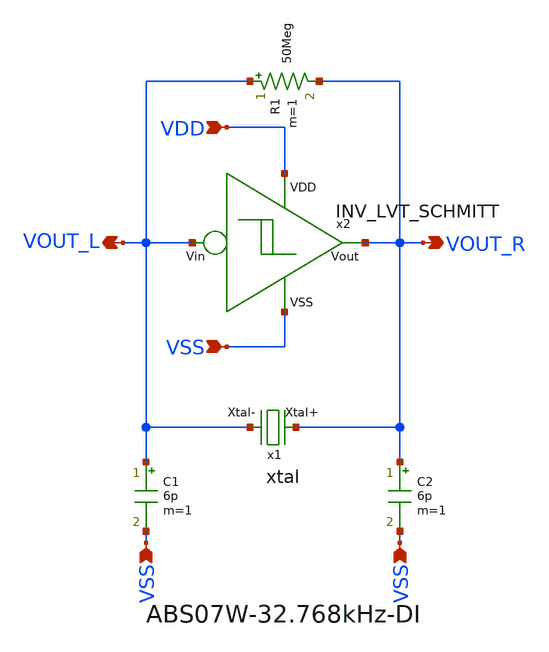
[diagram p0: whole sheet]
** sch_path: design/THESIS_EXP_RO_INVERTER_SKY130A/xtal_osc_schmitt.sch
**.subckt xtal_osc_schmitt VDD VSS VSS VSS VOUT_R VOUT_L
*.ipin VDD
*.ipin VSS
*.ipin VSS
*.ipin VSS
*.opin VOUT_R
*.opin VOUT_L
x1 VOUT_R VOUT_L xtal
C1 VOUT_L VSS 6p m=1
C2 VOUT_R VSS 6p m=1
R1 VOUT_L VOUT_R 50Meg m=1
x2 VDD VSS VOUT_R VOUT_L INV_LVT_SCHMITT
**.ends

* expanding   symbol:  THESIS_EXP_RO_INVERTER_SKY130A/xtal.sym # of pins=2
** sym_path: design/THESIS_EXP_RO_INVERTER_SKY130A/xtal.sym
** sch_path: design/THESIS_EXP_RO_INVERTER_SKY130A/xtal.sch
.subckt xtal Xtal+ Xtal-
*.iopin Xtal+
*.iopin Xtal-
R1 Xtal+ net1 38.194k m=1
C1 net1 net2 4.68f m=1
L1 net2 Xtal- 5048.571 m=1
C2 Xtal+ Xtal- 1.15p m=1
.ends


* expanding   symbol:  THESIS_EXP_RO_INVERTER_SKY130A/INV_LVT_SCHMITT.sym # of pins=4
** sym_path: design/THESIS_EXP_RO_INVERTER_SKY130A/INV_LVT_SCHMITT.sym
** sch_path: design/THESIS_EXP_RO_INVERTER_SKY130A/INV_LVT_SCHMITT.sch
.subckt INV_LVT_SCHMITT VDD VSS Vout Vin
*.ipin VSS
*.ipin Vin
*.opin Vout
*.ipin VDD
XM1[55] net1[13] Vin VDD VDD sky130_fd_pr__pfet_01v8_lvt L=1 W=7 nf=1 ad='int((nf+1)/2) * W/nf * 0.29'
+ as='int((nf+2)/2) * W/nf * 0.29' pd='2*int((nf+1)/2) * (W/nf + 0.29)' ps='2*int((nf+2)/2) * (W/nf + 0.29)'
+ nrd='0.29 / W' nrs='0.29 / W' sa=0 sb=0 sd=0 mult=1 m=1
XM1[54] net1[12] Vin VDD VDD sky130_fd_pr__pfet_01v8_lvt L=1 W=7 nf=1 ad='int((nf+1)/2) * W/nf * 0.29'
+ as='int((nf+2)/2) * W/nf * 0.29' pd='2*int((nf+1)/2) * (W/nf + 0.29)' ps='2*int((nf+2)/2) * (W/nf + 0.29)'
+ nrd='0.29 / W' nrs='0.29 / W' sa=0 sb=0 sd=0 mult=1 m=1
XM1[53] net1[11] Vin VDD VDD sky130_fd_pr__pfet_01v8_lvt L=1 W=7 nf=1 ad='int((nf+1)/2) * W/nf * 0.29'
+ as='int((nf+2)/2) * W/nf * 0.29' pd='2*int((nf+1)/2) * (W/nf + 0.29)' ps='2*int((nf+2)/2) * (W/nf + 0.29)'
+ nrd='0.29 / W' nrs='0.29 / W' sa=0 sb=0 sd=0 mult=1 m=1
XM1[52] net1[10] Vin VDD VDD sky130_fd_pr__pfet_01v8_lvt L=1 W=7 nf=1 ad='int((nf+1)/2) * W/nf * 0.29'
+ as='int((nf+2)/2) * W/nf * 0.29' pd='2*int((nf+1)/2) * (W/nf + 0.29)' ps='2*int((nf+2)/2) * (W/nf + 0.29)'
+ nrd='0.29 / W' nrs='0.29 / W' sa=0 sb=0 sd=0 mult=1 m=1
XM1[51] net1[9] Vin VDD VDD sky130_fd_pr__pfet_01v8_lvt L=1 W=7 nf=1 ad='int((nf+1)/2) * W/nf * 0.29'
+ as='int((nf+2)/2) * W/nf * 0.29' pd='2*int((nf+1)/2) * (W/nf + 0.29)' ps='2*int((nf+2)/2) * (W/nf + 0.29)'
+ nrd='0.29 / W' nrs='0.29 / W' sa=0 sb=0 sd=0 mult=1 m=1
XM1[50] net1[8] Vin VDD VDD sky130_fd_pr__pfet_01v8_lvt L=1 W=7 nf=1 ad='int((nf+1)/2) * W/nf * 0.29'
+ as='int((nf+2)/2) * W/nf * 0.29' pd='2*int((nf+1)/2) * (W/nf + 0.29)' ps='2*int((nf+2)/2) * (W/nf + 0.29)'
+ nrd='0.29 / W' nrs='0.29 / W' sa=0 sb=0 sd=0 mult=1 m=1
XM1[49] net1[7] Vin VDD VDD sky130_fd_pr__pfet_01v8_lvt L=1 W=7 nf=1 ad='int((nf+1)/2) * W/nf * 0.29'
+ as='int((nf+2)/2) * W/nf * 0.29' pd='2*int((nf+1)/2) * (W/nf + 0.29)' ps='2*int((nf+2)/2) * (W/nf + 0.29)'
+ nrd='0.29 / W' nrs='0.29 / W' sa=0 sb=0 sd=0 mult=1 m=1
XM1[48] net1[6] Vin VDD VDD sky130_fd_pr__pfet_01v8_lvt L=1 W=7 nf=1 ad='int((nf+1)/2) * W/nf * 0.29'
+ as='int((nf+2)/2) * W/nf * 0.29' pd='2*int((nf+1)/2) * (W/nf + 0.29)' ps='2*int((nf+2)/2) * (W/nf + 0.29)'
+ nrd='0.29 / W' nrs='0.29 / W' sa=0 sb=0 sd=0 mult=1 m=1
XM1[47] net1[5] Vin VDD VDD sky130_fd_pr__pfet_01v8_lvt L=1 W=7 nf=1 ad='int((nf+1)/2) * W/nf * 0.29'
+ as='int((nf+2)/2) * W/nf * 0.29' pd='2*int((nf+1)/2) * (W/nf + 0.29)' ps='2*int((nf+2)/2) * (W/nf + 0.29)'
+ nrd='0.29 / W' nrs='0.29 / W' sa=0 sb=0 sd=0 mult=1 m=1
XM1[46] net1[4] Vin VDD VDD sky130_fd_pr__pfet_01v8_lvt L=1 W=7 nf=1 ad='int((nf+1)/2) * W/nf * 0.29'
+ as='int((nf+2)/2) * W/nf * 0.29' pd='2*int((nf+1)/2) * (W/nf + 0.29)' ps='2*int((nf+2)/2) * (W/nf + 0.29)'
+ nrd='0.29 / W' nrs='0.29 / W' sa=0 sb=0 sd=0 mult=1 m=1
XM1[45] net1[3] Vin VDD VDD sky130_fd_pr__pfet_01v8_lvt L=1 W=7 nf=1 ad='int((nf+1)/2) * W/nf * 0.29'
+ as='int((nf+2)/2) * W/nf * 0.29' pd='2*int((nf+1)/2) * (W/nf + 0.29)' ps='2*int((nf+2)/2) * (W/nf + 0.29)'
+ nrd='0.29 / W' nrs='0.29 / W' sa=0 sb=0 sd=0 mult=1 m=1
XM1[44] net1[2] Vin VDD VDD sky130_fd_pr__pfet_01v8_lvt L=1 W=7 nf=1 ad='int((nf+1)/2) * W/nf * 0.29'
+ as='int((nf+2)/2) * W/nf * 0.29' pd='2*int((nf+1)/2) * (W/nf + 0.29)' ps='2*int((nf+2)/2) * (W/nf + 0.29)'
+ nrd='0.29 / W' nrs='0.29 / W' sa=0 sb=0 sd=0 mult=1 m=1
XM1[43] net1[1] Vin VDD VDD sky130_fd_pr__pfet_01v8_lvt L=1 W=7 nf=1 ad='int((nf+1)/2) * W/nf * 0.29'
+ as='int((nf+2)/2) * W/nf * 0.29' pd='2*int((nf+1)/2) * (W/nf + 0.29)' ps='2*int((nf+2)/2) * (W/nf + 0.29)'
+ nrd='0.29 / W' nrs='0.29 / W' sa=0 sb=0 sd=0 mult=1 m=1
XM1[42] net1[0] Vin VDD VDD sky130_fd_pr__pfet_01v8_lvt L=1 W=7 nf=1 ad='int((nf+1)/2) * W/nf * 0.29'
+ as='int((nf+2)/2) * W/nf * 0.29' pd='2*int((nf+1)/2) * (W/nf + 0.29)' ps='2*int((nf+2)/2) * (W/nf + 0.29)'
+ nrd='0.29 / W' nrs='0.29 / W' sa=0 sb=0 sd=0 mult=1 m=1
XM1[41] net1[13] Vin VDD VDD sky130_fd_pr__pfet_01v8_lvt L=1 W=7 nf=1 ad='int((nf+1)/2) * W/nf * 0.29'
+ as='int((nf+2)/2) * W/nf * 0.29' pd='2*int((nf+1)/2) * (W/nf + 0.29)' ps='2*int((nf+2)/2) * (W/nf + 0.29)'
+ nrd='0.29 / W' nrs='0.29 / W' sa=0 sb=0 sd=0 mult=1 m=1
XM1[40] net1[12] Vin VDD VDD sky130_fd_pr__pfet_01v8_lvt L=1 W=7 nf=1 ad='int((nf+1)/2) * W/nf * 0.29'
+ as='int((nf+2)/2) * W/nf * 0.29' pd='2*int((nf+1)/2) * (W/nf + 0.29)' ps='2*int((nf+2)/2) * (W/nf + 0.29)'
+ nrd='0.29 / W' nrs='0.29 / W' sa=0 sb=0 sd=0 mult=1 m=1
XM1[39] net1[11] Vin VDD VDD sky130_fd_pr__pfet_01v8_lvt L=1 W=7 nf=1 ad='int((nf+1)/2) * W/nf * 0.29'
+ as='int((nf+2)/2) * W/nf * 0.29' pd='2*int((nf+1)/2) * (W/nf + 0.29)' ps='2*int((nf+2)/2) * (W/nf + 0.29)'
+ nrd='0.29 / W' nrs='0.29 / W' sa=0 sb=0 sd=0 mult=1 m=1
XM1[38] net1[10] Vin VDD VDD sky130_fd_pr__pfet_01v8_lvt L=1 W=7 nf=1 ad='int((nf+1)/2) * W/nf * 0.29'
+ as='int((nf+2)/2) * W/nf * 0.29' pd='2*int((nf+1)/2) * (W/nf + 0.29)' ps='2*int((nf+2)/2) * (W/nf + 0.29)'
+ nrd='0.29 / W' nrs='0.29 / W' sa=0 sb=0 sd=0 mult=1 m=1
XM1[37] net1[9] Vin VDD VDD sky130_fd_pr__pfet_01v8_lvt L=1 W=7 nf=1 ad='int((nf+1)/2) * W/nf * 0.29'
+ as='int((nf+2)/2) * W/nf * 0.29' pd='2*int((nf+1)/2) * (W/nf + 0.29)' ps='2*int((nf+2)/2) * (W/nf + 0.29)'
+ nrd='0.29 / W' nrs='0.29 / W' sa=0 sb=0 sd=0 mult=1 m=1
XM1[36] net1[8] Vin VDD VDD sky130_fd_pr__pfet_01v8_lvt L=1 W=7 nf=1 ad='int((nf+1)/2) * W/nf * 0.29'
+ as='int((nf+2)/2) * W/nf * 0.29' pd='2*int((nf+1)/2) * (W/nf + 0.29)' ps='2*int((nf+2)/2) * (W/nf + 0.29)'
+ nrd='0.29 / W' nrs='0.29 / W' sa=0 sb=0 sd=0 mult=1 m=1
XM1[35] net1[7] Vin VDD VDD sky130_fd_pr__pfet_01v8_lvt L=1 W=7 nf=1 ad='int((nf+1)/2) * W/nf * 0.29'
+ as='int((nf+2)/2) * W/nf * 0.29' pd='2*int((nf+1)/2) * (W/nf + 0.29)' ps='2*int((nf+2)/2) * (W/nf + 0.29)'
+ nrd='0.29 / W' nrs='0.29 / W' sa=0 sb=0 sd=0 mult=1 m=1
XM1[34] net1[6] Vin VDD VDD sky130_fd_pr__pfet_01v8_lvt L=1 W=7 nf=1 ad='int((nf+1)/2) * W/nf * 0.29'
+ as='int((nf+2)/2) * W/nf * 0.29' pd='2*int((nf+1)/2) * (W/nf + 0.29)' ps='2*int((nf+2)/2) * (W/nf + 0.29)'
+ nrd='0.29 / W' nrs='0.29 / W' sa=0 sb=0 sd=0 mult=1 m=1
XM1[33] net1[5] Vin VDD VDD sky130_fd_pr__pfet_01v8_lvt L=1 W=7 nf=1 ad='int((nf+1)/2) * W/nf * 0.29'
+ as='int((nf+2)/2) * W/nf * 0.29' pd='2*int((nf+1)/2) * (W/nf + 0.29)' ps='2*int((nf+2)/2) * (W/nf + 0.29)'
+ nrd='0.29 / W' nrs='0.29 / W' sa=0 sb=0 sd=0 mult=1 m=1
XM1[32] net1[4] Vin VDD VDD sky130_fd_pr__pfet_01v8_lvt L=1 W=7 nf=1 ad='int((nf+1)/2) * W/nf * 0.29'
+ as='int((nf+2)/2) * W/nf * 0.29' pd='2*int((nf+1)/2) * (W/nf + 0.29)' ps='2*int((nf+2)/2) * (W/nf + 0.29)'
+ nrd='0.29 / W' nrs='0.29 / W' sa=0 sb=0 sd=0 mult=1 m=1
XM1[31] net1[3] Vin VDD VDD sky130_fd_pr__pfet_01v8_lvt L=1 W=7 nf=1 ad='int((nf+1)/2) * W/nf * 0.29'
+ as='int((nf+2)/2) * W/nf * 0.29' pd='2*int((nf+1)/2) * (W/nf + 0.29)' ps='2*int((nf+2)/2) * (W/nf + 0.29)'
+ nrd='0.29 / W' nrs='0.29 / W' sa=0 sb=0 sd=0 mult=1 m=1
XM1[30] net1[2] Vin VDD VDD sky130_fd_pr__pfet_01v8_lvt L=1 W=7 nf=1 ad='int((nf+1)/2) * W/nf * 0.29'
+ as='int((nf+2)/2) * W/nf * 0.29' pd='2*int((nf+1)/2) * (W/nf + 0.29)' ps='2*int((nf+2)/2) * (W/nf + 0.29)'
+ nrd='0.29 / W' nrs='0.29 / W' sa=0 sb=0 sd=0 mult=1 m=1
XM1[29] net1[1] Vin VDD VDD sky130_fd_pr__pfet_01v8_lvt L=1 W=7 nf=1 ad='int((nf+1)/2) * W/nf * 0.29'
+ as='int((nf+2)/2) * W/nf * 0.29' pd='2*int((nf+1)/2) * (W/nf + 0.29)' ps='2*int((nf+2)/2) * (W/nf + 0.29)'
+ nrd='0.29 / W' nrs='0.29 / W' sa=0 sb=0 sd=0 mult=1 m=1
XM1[28] net1[0] Vin VDD VDD sky130_fd_pr__pfet_01v8_lvt L=1 W=7 nf=1 ad='int((nf+1)/2) * W/nf * 0.29'
+ as='int((nf+2)/2) * W/nf * 0.29' pd='2*int((nf+1)/2) * (W/nf + 0.29)' ps='2*int((nf+2)/2) * (W/nf + 0.29)'
+ nrd='0.29 / W' nrs='0.29 / W' sa=0 sb=0 sd=0 mult=1 m=1
XM1[27] net1[13] Vin VDD VDD sky130_fd_pr__pfet_01v8_lvt L=1 W=7 nf=1 ad='int((nf+1)/2) * W/nf * 0.29'
+ as='int((nf+2)/2) * W/nf * 0.29' pd='2*int((nf+1)/2) * (W/nf + 0.29)' ps='2*int((nf+2)/2) * (W/nf + 0.29)'
+ nrd='0.29 / W' nrs='0.29 / W' sa=0 sb=0 sd=0 mult=1 m=1
XM1[26] net1[12] Vin VDD VDD sky130_fd_pr__pfet_01v8_lvt L=1 W=7 nf=1 ad='int((nf+1)/2) * W/nf * 0.29'
+ as='int((nf+2)/2) * W/nf * 0.29' pd='2*int((nf+1)/2) * (W/nf + 0.29)' ps='2*int((nf+2)/2) * (W/nf + 0.29)'
+ nrd='0.29 / W' nrs='0.29 / W' sa=0 sb=0 sd=0 mult=1 m=1
XM1[25] net1[11] Vin VDD VDD sky130_fd_pr__pfet_01v8_lvt L=1 W=7 nf=1 ad='int((nf+1)/2) * W/nf * 0.29'
+ as='int((nf+2)/2) * W/nf * 0.29' pd='2*int((nf+1)/2) * (W/nf + 0.29)' ps='2*int((nf+2)/2) * (W/nf + 0.29)'
+ nrd='0.29 / W' nrs='0.29 / W' sa=0 sb=0 sd=0 mult=1 m=1
XM1[24] net1[10] Vin VDD VDD sky130_fd_pr__pfet_01v8_lvt L=1 W=7 nf=1 ad='int((nf+1)/2) * W/nf * 0.29'
+ as='int((nf+2)/2) * W/nf * 0.29' pd='2*int((nf+1)/2) * (W/nf + 0.29)' ps='2*int((nf+2)/2) * (W/nf + 0.29)'
+ nrd='0.29 / W' nrs='0.29 / W' sa=0 sb=0 sd=0 mult=1 m=1
XM1[23] net1[9] Vin VDD VDD sky130_fd_pr__pfet_01v8_lvt L=1 W=7 nf=1 ad='int((nf+1)/2) * W/nf * 0.29'
+ as='int((nf+2)/2) * W/nf * 0.29' pd='2*int((nf+1)/2) * (W/nf + 0.29)' ps='2*int((nf+2)/2) * (W/nf + 0.29)'
+ nrd='0.29 / W' nrs='0.29 / W' sa=0 sb=0 sd=0 mult=1 m=1
XM1[22] net1[8] Vin VDD VDD sky130_fd_pr__pfet_01v8_lvt L=1 W=7 nf=1 ad='int((nf+1)/2) * W/nf * 0.29'
+ as='int((nf+2)/2) * W/nf * 0.29' pd='2*int((nf+1)/2) * (W/nf + 0.29)' ps='2*int((nf+2)/2) * (W/nf + 0.29)'
+ nrd='0.29 / W' nrs='0.29 / W' sa=0 sb=0 sd=0 mult=1 m=1
XM1[21] net1[7] Vin VDD VDD sky130_fd_pr__pfet_01v8_lvt L=1 W=7 nf=1 ad='int((nf+1)/2) * W/nf * 0.29'
+ as='int((nf+2)/2) * W/nf * 0.29' pd='2*int((nf+1)/2) * (W/nf + 0.29)' ps='2*int((nf+2)/2) * (W/nf + 0.29)'
+ nrd='0.29 / W' nrs='0.29 / W' sa=0 sb=0 sd=0 mult=1 m=1
XM1[20] net1[6] Vin VDD VDD sky130_fd_pr__pfet_01v8_lvt L=1 W=7 nf=1 ad='int((nf+1)/2) * W/nf * 0.29'
+ as='int((nf+2)/2) * W/nf * 0.29' pd='2*int((nf+1)/2) * (W/nf + 0.29)' ps='2*int((nf+2)/2) * (W/nf + 0.29)'
+ nrd='0.29 / W' nrs='0.29 / W' sa=0 sb=0 sd=0 mult=1 m=1
XM1[19] net1[5] Vin VDD VDD sky130_fd_pr__pfet_01v8_lvt L=1 W=7 nf=1 ad='int((nf+1)/2) * W/nf * 0.29'
+ as='int((nf+2)/2) * W/nf * 0.29' pd='2*int((nf+1)/2) * (W/nf + 0.29)' ps='2*int((nf+2)/2) * (W/nf + 0.29)'
+ nrd='0.29 / W' nrs='0.29 / W' sa=0 sb=0 sd=0 mult=1 m=1
XM1[18] net1[4] Vin VDD VDD sky130_fd_pr__pfet_01v8_lvt L=1 W=7 nf=1 ad='int((nf+1)/2) * W/nf * 0.29'
+ as='int((nf+2)/2) * W/nf * 0.29' pd='2*int((nf+1)/2) * (W/nf + 0.29)' ps='2*int((nf+2)/2) * (W/nf + 0.29)'
+ nrd='0.29 / W' nrs='0.29 / W' sa=0 sb=0 sd=0 mult=1 m=1
XM1[17] net1[3] Vin VDD VDD sky130_fd_pr__pfet_01v8_lvt L=1 W=7 nf=1 ad='int((nf+1)/2) * W/nf * 0.29'
+ as='int((nf+2)/2) * W/nf * 0.29' pd='2*int((nf+1)/2) * (W/nf + 0.29)' ps='2*int((nf+2)/2) * (W/nf + 0.29)'
+ nrd='0.29 / W' nrs='0.29 / W' sa=0 sb=0 sd=0 mult=1 m=1
XM1[16] net1[2] Vin VDD VDD sky130_fd_pr__pfet_01v8_lvt L=1 W=7 nf=1 ad='int((nf+1)/2) * W/nf * 0.29'
+ as='int((nf+2)/2) * W/nf * 0.29' pd='2*int((nf+1)/2) * (W/nf + 0.29)' ps='2*int((nf+2)/2) * (W/nf + 0.29)'
+ nrd='0.29 / W' nrs='0.29 / W' sa=0 sb=0 sd=0 mult=1 m=1
XM1[15] net1[1] Vin VDD VDD sky130_fd_pr__pfet_01v8_lvt L=1 W=7 nf=1 ad='int((nf+1)/2) * W/nf * 0.29'
+ as='int((nf+2)/2) * W/nf * 0.29' pd='2*int((nf+1)/2) * (W/nf + 0.29)' ps='2*int((nf+2)/2) * (W/nf + 0.29)'
+ nrd='0.29 / W' nrs='0.29 / W' sa=0 sb=0 sd=0 mult=1 m=1
XM1[14] net1[0] Vin VDD VDD sky130_fd_pr__pfet_01v8_lvt L=1 W=7 nf=1 ad='int((nf+1)/2) * W/nf * 0.29'
+ as='int((nf+2)/2) * W/nf * 0.29' pd='2*int((nf+1)/2) * (W/nf + 0.29)' ps='2*int((nf+2)/2) * (W/nf + 0.29)'
+ nrd='0.29 / W' nrs='0.29 / W' sa=0 sb=0 sd=0 mult=1 m=1
XM1[13] net1[13] Vin VDD VDD sky130_fd_pr__pfet_01v8_lvt L=1 W=7 nf=1 ad='int((nf+1)/2) * W/nf * 0.29'
+ as='int((nf+2)/2) * W/nf * 0.29' pd='2*int((nf+1)/2) * (W/nf + 0.29)' ps='2*int((nf+2)/2) * (W/nf + 0.29)'
+ nrd='0.29 / W' nrs='0.29 / W' sa=0 sb=0 sd=0 mult=1 m=1
XM1[12] net1[12] Vin VDD VDD sky130_fd_pr__pfet_01v8_lvt L=1 W=7 nf=1 ad='int((nf+1)/2) * W/nf * 0.29'
+ as='int((nf+2)/2) * W/nf * 0.29' pd='2*int((nf+1)/2) * (W/nf + 0.29)' ps='2*int((nf+2)/2) * (W/nf + 0.29)'
+ nrd='0.29 / W' nrs='0.29 / W' sa=0 sb=0 sd=0 mult=1 m=1
XM1[11] net1[11] Vin VDD VDD sky130_fd_pr__pfet_01v8_lvt L=1 W=7 nf=1 ad='int((nf+1)/2) * W/nf * 0.29'
+ as='int((nf+2)/2) * W/nf * 0.29' pd='2*int((nf+1)/2) * (W/nf + 0.29)' ps='2*int((nf+2)/2) * (W/nf + 0.29)'
+ nrd='0.29 / W' nrs='0.29 / W' sa=0 sb=0 sd=0 mult=1 m=1
XM1[10] net1[10] Vin VDD VDD sky130_fd_pr__pfet_01v8_lvt L=1 W=7 nf=1 ad='int((nf+1)/2) * W/nf * 0.29'
+ as='int((nf+2)/2) * W/nf * 0.29' pd='2*int((nf+1)/2) * (W/nf + 0.29)' ps='2*int((nf+2)/2) * (W/nf + 0.29)'
+ nrd='0.29 / W' nrs='0.29 / W' sa=0 sb=0 sd=0 mult=1 m=1
XM1[9] net1[9] Vin VDD VDD sky130_fd_pr__pfet_01v8_lvt L=1 W=7 nf=1 ad='int((nf+1)/2) * W/nf * 0.29'
+ as='int((nf+2)/2) * W/nf * 0.29' pd='2*int((nf+1)/2) * (W/nf + 0.29)' ps='2*int((nf+2)/2) * (W/nf + 0.29)'
+ nrd='0.29 / W' nrs='0.29 / W' sa=0 sb=0 sd=0 mult=1 m=1
XM1[8] net1[8] Vin VDD VDD sky130_fd_pr__pfet_01v8_lvt L=1 W=7 nf=1 ad='int((nf+1)/2) * W/nf * 0.29'
+ as='int((nf+2)/2) * W/nf * 0.29' pd='2*int((nf+1)/2) * (W/nf + 0.29)' ps='2*int((nf+2)/2) * (W/nf + 0.29)'
+ nrd='0.29 / W' nrs='0.29 / W' sa=0 sb=0 sd=0 mult=1 m=1
XM1[7] net1[7] Vin VDD VDD sky130_fd_pr__pfet_01v8_lvt L=1 W=7 nf=1 ad='int((nf+1)/2) * W/nf * 0.29'
+ as='int((nf+2)/2) * W/nf * 0.29' pd='2*int((nf+1)/2) * (W/nf + 0.29)' ps='2*int((nf+2)/2) * (W/nf + 0.29)'
+ nrd='0.29 / W' nrs='0.29 / W' sa=0 sb=0 sd=0 mult=1 m=1
XM1[6] net1[6] Vin VDD VDD sky130_fd_pr__pfet_01v8_lvt L=1 W=7 nf=1 ad='int((nf+1)/2) * W/nf * 0.29'
+ as='int((nf+2)/2) * W/nf * 0.29' pd='2*int((nf+1)/2) * (W/nf + 0.29)' ps='2*int((nf+2)/2) * (W/nf + 0.29)'
+ nrd='0.29 / W' nrs='0.29 / W' sa=0 sb=0 sd=0 mult=1 m=1
XM1[5] net1[5] Vin VDD VDD sky130_fd_pr__pfet_01v8_lvt L=1 W=7 nf=1 ad='int((nf+1)/2) * W/nf * 0.29'
+ as='int((nf+2)/2) * W/nf * 0.29' pd='2*int((nf+1)/2) * (W/nf + 0.29)' ps='2*int((nf+2)/2) * (W/nf + 0.29)'
+ nrd='0.29 / W' nrs='0.29 / W' sa=0 sb=0 sd=0 mult=1 m=1
XM1[4] net1[4] Vin VDD VDD sky130_fd_pr__pfet_01v8_lvt L=1 W=7 nf=1 ad='int((nf+1)/2) * W/nf * 0.29'
+ as='int((nf+2)/2) * W/nf * 0.29' pd='2*int((nf+1)/2) * (W/nf + 0.29)' ps='2*int((nf+2)/2) * (W/nf + 0.29)'
+ nrd='0.29 / W' nrs='0.29 / W' sa=0 sb=0 sd=0 mult=1 m=1
XM1[3] net1[3] Vin VDD VDD sky130_fd_pr__pfet_01v8_lvt L=1 W=7 nf=1 ad='int((nf+1)/2) * W/nf * 0.29'
+ as='int((nf+2)/2) * W/nf * 0.29' pd='2*int((nf+1)/2) * (W/nf + 0.29)' ps='2*int((nf+2)/2) * (W/nf + 0.29)'
+ nrd='0.29 / W' nrs='0.29 / W' sa=0 sb=0 sd=0 mult=1 m=1
XM1[2] net1[2] Vin VDD VDD sky130_fd_pr__pfet_01v8_lvt L=1 W=7 nf=1 ad='int((nf+1)/2) * W/nf * 0.29'
+ as='int((nf+2)/2) * W/nf * 0.29' pd='2*int((nf+1)/2) * (W/nf + 0.29)' ps='2*int((nf+2)/2) * (W/nf + 0.29)'
+ nrd='0.29 / W' nrs='0.29 / W' sa=0 sb=0 sd=0 mult=1 m=1
XM1[1] net1[1] Vin VDD VDD sky130_fd_pr__pfet_01v8_lvt L=1 W=7 nf=1 ad='int((nf+1)/2) * W/nf * 0.29'
+ as='int((nf+2)/2) * W/nf * 0.29' pd='2*int((nf+1)/2) * (W/nf + 0.29)' ps='2*int((nf+2)/2) * (W/nf + 0.29)'
+ nrd='0.29 / W' nrs='0.29 / W' sa=0 sb=0 sd=0 mult=1 m=1
XM1[0] net1[0] Vin VDD VDD sky130_fd_pr__pfet_01v8_lvt L=1 W=7 nf=1 ad='int((nf+1)/2) * W/nf * 0.29'
+ as='int((nf+2)/2) * W/nf * 0.29' pd='2*int((nf+1)/2) * (W/nf + 0.29)' ps='2*int((nf+2)/2) * (W/nf + 0.29)'
+ nrd='0.29 / W' nrs='0.29 / W' sa=0 sb=0 sd=0 mult=1 m=1
XM2[13] Vout Vin net1[13] VDD sky130_fd_pr__pfet_01v8_lvt L=1 W=7 nf=1 ad='int((nf+1)/2) * W/nf * 0.29'
+ as='int((nf+2)/2) * W/nf * 0.29' pd='2*int((nf+1)/2) * (W/nf + 0.29)' ps='2*int((nf+2)/2) * (W/nf + 0.29)'
+ nrd='0.29 / W' nrs='0.29 / W' sa=0 sb=0 sd=0 mult=1 m=1
XM2[12] Vout Vin net1[12] VDD sky130_fd_pr__pfet_01v8_lvt L=1 W=7 nf=1 ad='int((nf+1)/2) * W/nf * 0.29'
+ as='int((nf+2)/2) * W/nf * 0.29' pd='2*int((nf+1)/2) * (W/nf + 0.29)' ps='2*int((nf+2)/2) * (W/nf + 0.29)'
+ nrd='0.29 / W' nrs='0.29 / W' sa=0 sb=0 sd=0 mult=1 m=1
XM2[11] Vout Vin net1[11] VDD sky130_fd_pr__pfet_01v8_lvt L=1 W=7 nf=1 ad='int((nf+1)/2) * W/nf * 0.29'
+ as='int((nf+2)/2) * W/nf * 0.29' pd='2*int((nf+1)/2) * (W/nf + 0.29)' ps='2*int((nf+2)/2) * (W/nf + 0.29)'
+ nrd='0.29 / W' nrs='0.29 / W' sa=0 sb=0 sd=0 mult=1 m=1
XM2[10] Vout Vin net1[10] VDD sky130_fd_pr__pfet_01v8_lvt L=1 W=7 nf=1 ad='int((nf+1)/2) * W/nf * 0.29'
+ as='int((nf+2)/2) * W/nf * 0.29' pd='2*int((nf+1)/2) * (W/nf + 0.29)' ps='2*int((nf+2)/2) * (W/nf + 0.29)'
+ nrd='0.29 / W' nrs='0.29 / W' sa=0 sb=0 sd=0 mult=1 m=1
XM2[9] Vout Vin net1[9] VDD sky130_fd_pr__pfet_01v8_lvt L=1 W=7 nf=1 ad='int((nf+1)/2) * W/nf * 0.29'
+ as='int((nf+2)/2) * W/nf * 0.29' pd='2*int((nf+1)/2) * (W/nf + 0.29)' ps='2*int((nf+2)/2) * (W/nf + 0.29)'
+ nrd='0.29 / W' nrs='0.29 / W' sa=0 sb=0 sd=0 mult=1 m=1
XM2[8] Vout Vin net1[8] VDD sky130_fd_pr__pfet_01v8_lvt L=1 W=7 nf=1 ad='int((nf+1)/2) * W/nf * 0.29'
+ as='int((nf+2)/2) * W/nf * 0.29' pd='2*int((nf+1)/2) * (W/nf + 0.29)' ps='2*int((nf+2)/2) * (W/nf + 0.29)'
+ nrd='0.29 / W' nrs='0.29 / W' sa=0 sb=0 sd=0 mult=1 m=1
XM2[7] Vout Vin net1[7] VDD sky130_fd_pr__pfet_01v8_lvt L=1 W=7 nf=1 ad='int((nf+1)/2) * W/nf * 0.29'
+ as='int((nf+2)/2) * W/nf * 0.29' pd='2*int((nf+1)/2) * (W/nf + 0.29)' ps='2*int((nf+2)/2) * (W/nf + 0.29)'
+ nrd='0.29 / W' nrs='0.29 / W' sa=0 sb=0 sd=0 mult=1 m=1
XM2[6] Vout Vin net1[6] VDD sky130_fd_pr__pfet_01v8_lvt L=1 W=7 nf=1 ad='int((nf+1)/2) * W/nf * 0.29'
+ as='int((nf+2)/2) * W/nf * 0.29' pd='2*int((nf+1)/2) * (W/nf + 0.29)' ps='2*int((nf+2)/2) * (W/nf + 0.29)'
+ nrd='0.29 / W' nrs='0.29 / W' sa=0 sb=0 sd=0 mult=1 m=1
XM2[5] Vout Vin net1[5] VDD sky130_fd_pr__pfet_01v8_lvt L=1 W=7 nf=1 ad='int((nf+1)/2) * W/nf * 0.29'
+ as='int((nf+2)/2) * W/nf * 0.29' pd='2*int((nf+1)/2) * (W/nf + 0.29)' ps='2*int((nf+2)/2) * (W/nf + 0.29)'
+ nrd='0.29 / W' nrs='0.29 / W' sa=0 sb=0 sd=0 mult=1 m=1
XM2[4] Vout Vin net1[4] VDD sky130_fd_pr__pfet_01v8_lvt L=1 W=7 nf=1 ad='int((nf+1)/2) * W/nf * 0.29'
+ as='int((nf+2)/2) * W/nf * 0.29' pd='2*int((nf+1)/2) * (W/nf + 0.29)' ps='2*int((nf+2)/2) * (W/nf + 0.29)'
+ nrd='0.29 / W' nrs='0.29 / W' sa=0 sb=0 sd=0 mult=1 m=1
XM2[3] Vout Vin net1[3] VDD sky130_fd_pr__pfet_01v8_lvt L=1 W=7 nf=1 ad='int((nf+1)/2) * W/nf * 0.29'
+ as='int((nf+2)/2) * W/nf * 0.29' pd='2*int((nf+1)/2) * (W/nf + 0.29)' ps='2*int((nf+2)/2) * (W/nf + 0.29)'
+ nrd='0.29 / W' nrs='0.29 / W' sa=0 sb=0 sd=0 mult=1 m=1
XM2[2] Vout Vin net1[2] VDD sky130_fd_pr__pfet_01v8_lvt L=1 W=7 nf=1 ad='int((nf+1)/2) * W/nf * 0.29'
+ as='int((nf+2)/2) * W/nf * 0.29' pd='2*int((nf+1)/2) * (W/nf + 0.29)' ps='2*int((nf+2)/2) * (W/nf + 0.29)'
+ nrd='0.29 / W' nrs='0.29 / W' sa=0 sb=0 sd=0 mult=1 m=1
XM2[1] Vout Vin net1[1] VDD sky130_fd_pr__pfet_01v8_lvt L=1 W=7 nf=1 ad='int((nf+1)/2) * W/nf * 0.29'
+ as='int((nf+2)/2) * W/nf * 0.29' pd='2*int((nf+1)/2) * (W/nf + 0.29)' ps='2*int((nf+2)/2) * (W/nf + 0.29)'
+ nrd='0.29 / W' nrs='0.29 / W' sa=0 sb=0 sd=0 mult=1 m=1
XM2[0] Vout Vin net1[0] VDD sky130_fd_pr__pfet_01v8_lvt L=1 W=7 nf=1 ad='int((nf+1)/2) * W/nf * 0.29'
+ as='int((nf+2)/2) * W/nf * 0.29' pd='2*int((nf+1)/2) * (W/nf + 0.29)' ps='2*int((nf+2)/2) * (W/nf + 0.29)'
+ nrd='0.29 / W' nrs='0.29 / W' sa=0 sb=0 sd=0 mult=1 m=1
XM3[27] net1[13] Vout VSS VDD sky130_fd_pr__pfet_01v8_lvt L=1 W=7 nf=1 ad='int((nf+1)/2) * W/nf * 0.29'
+ as='int((nf+2)/2) * W/nf * 0.29' pd='2*int((nf+1)/2) * (W/nf + 0.29)' ps='2*int((nf+2)/2) * (W/nf + 0.29)'
+ nrd='0.29 / W' nrs='0.29 / W' sa=0 sb=0 sd=0 mult=1 m=1
XM3[26] net1[12] Vout VSS VDD sky130_fd_pr__pfet_01v8_lvt L=1 W=7 nf=1 ad='int((nf+1)/2) * W/nf * 0.29'
+ as='int((nf+2)/2) * W/nf * 0.29' pd='2*int((nf+1)/2) * (W/nf + 0.29)' ps='2*int((nf+2)/2) * (W/nf + 0.29)'
+ nrd='0.29 / W' nrs='0.29 / W' sa=0 sb=0 sd=0 mult=1 m=1
XM3[25] net1[11] Vout VSS VDD sky130_fd_pr__pfet_01v8_lvt L=1 W=7 nf=1 ad='int((nf+1)/2) * W/nf * 0.29'
+ as='int((nf+2)/2) * W/nf * 0.29' pd='2*int((nf+1)/2) * (W/nf + 0.29)' ps='2*int((nf+2)/2) * (W/nf + 0.29)'
+ nrd='0.29 / W' nrs='0.29 / W' sa=0 sb=0 sd=0 mult=1 m=1
XM3[24] net1[10] Vout VSS VDD sky130_fd_pr__pfet_01v8_lvt L=1 W=7 nf=1 ad='int((nf+1)/2) * W/nf * 0.29'
+ as='int((nf+2)/2) * W/nf * 0.29' pd='2*int((nf+1)/2) * (W/nf + 0.29)' ps='2*int((nf+2)/2) * (W/nf + 0.29)'
+ nrd='0.29 / W' nrs='0.29 / W' sa=0 sb=0 sd=0 mult=1 m=1
XM3[23] net1[9] Vout VSS VDD sky130_fd_pr__pfet_01v8_lvt L=1 W=7 nf=1 ad='int((nf+1)/2) * W/nf * 0.29'
+ as='int((nf+2)/2) * W/nf * 0.29' pd='2*int((nf+1)/2) * (W/nf + 0.29)' ps='2*int((nf+2)/2) * (W/nf + 0.29)'
+ nrd='0.29 / W' nrs='0.29 / W' sa=0 sb=0 sd=0 mult=1 m=1
XM3[22] net1[8] Vout VSS VDD sky130_fd_pr__pfet_01v8_lvt L=1 W=7 nf=1 ad='int((nf+1)/2) * W/nf * 0.29'
+ as='int((nf+2)/2) * W/nf * 0.29' pd='2*int((nf+1)/2) * (W/nf + 0.29)' ps='2*int((nf+2)/2) * (W/nf + 0.29)'
+ nrd='0.29 / W' nrs='0.29 / W' sa=0 sb=0 sd=0 mult=1 m=1
XM3[21] net1[7] Vout VSS VDD sky130_fd_pr__pfet_01v8_lvt L=1 W=7 nf=1 ad='int((nf+1)/2) * W/nf * 0.29'
+ as='int((nf+2)/2) * W/nf * 0.29' pd='2*int((nf+1)/2) * (W/nf + 0.29)' ps='2*int((nf+2)/2) * (W/nf + 0.29)'
+ nrd='0.29 / W' nrs='0.29 / W' sa=0 sb=0 sd=0 mult=1 m=1
XM3[20] net1[6] Vout VSS VDD sky130_fd_pr__pfet_01v8_lvt L=1 W=7 nf=1 ad='int((nf+1)/2) * W/nf * 0.29'
+ as='int((nf+2)/2) * W/nf * 0.29' pd='2*int((nf+1)/2) * (W/nf + 0.29)' ps='2*int((nf+2)/2) * (W/nf + 0.29)'
+ nrd='0.29 / W' nrs='0.29 / W' sa=0 sb=0 sd=0 mult=1 m=1
XM3[19] net1[5] Vout VSS VDD sky130_fd_pr__pfet_01v8_lvt L=1 W=7 nf=1 ad='int((nf+1)/2) * W/nf * 0.29'
+ as='int((nf+2)/2) * W/nf * 0.29' pd='2*int((nf+1)/2) * (W/nf + 0.29)' ps='2*int((nf+2)/2) * (W/nf + 0.29)'
+ nrd='0.29 / W' nrs='0.29 / W' sa=0 sb=0 sd=0 mult=1 m=1
XM3[18] net1[4] Vout VSS VDD sky130_fd_pr__pfet_01v8_lvt L=1 W=7 nf=1 ad='int((nf+1)/2) * W/nf * 0.29'
+ as='int((nf+2)/2) * W/nf * 0.29' pd='2*int((nf+1)/2) * (W/nf + 0.29)' ps='2*int((nf+2)/2) * (W/nf + 0.29)'
+ nrd='0.29 / W' nrs='0.29 / W' sa=0 sb=0 sd=0 mult=1 m=1
XM3[17] net1[3] Vout VSS VDD sky130_fd_pr__pfet_01v8_lvt L=1 W=7 nf=1 ad='int((nf+1)/2) * W/nf * 0.29'
+ as='int((nf+2)/2) * W/nf * 0.29' pd='2*int((nf+1)/2) * (W/nf + 0.29)' ps='2*int((nf+2)/2) * (W/nf + 0.29)'
+ nrd='0.29 / W' nrs='0.29 / W' sa=0 sb=0 sd=0 mult=1 m=1
XM3[16] net1[2] Vout VSS VDD sky130_fd_pr__pfet_01v8_lvt L=1 W=7 nf=1 ad='int((nf+1)/2) * W/nf * 0.29'
+ as='int((nf+2)/2) * W/nf * 0.29' pd='2*int((nf+1)/2) * (W/nf + 0.29)' ps='2*int((nf+2)/2) * (W/nf + 0.29)'
+ nrd='0.29 / W' nrs='0.29 / W' sa=0 sb=0 sd=0 mult=1 m=1
XM3[15] net1[1] Vout VSS VDD sky130_fd_pr__pfet_01v8_lvt L=1 W=7 nf=1 ad='int((nf+1)/2) * W/nf * 0.29'
+ as='int((nf+2)/2) * W/nf * 0.29' pd='2*int((nf+1)/2) * (W/nf + 0.29)' ps='2*int((nf+2)/2) * (W/nf + 0.29)'
+ nrd='0.29 / W' nrs='0.29 / W' sa=0 sb=0 sd=0 mult=1 m=1
XM3[14] net1[0] Vout VSS VDD sky130_fd_pr__pfet_01v8_lvt L=1 W=7 nf=1 ad='int((nf+1)/2) * W/nf * 0.29'
+ as='int((nf+2)/2) * W/nf * 0.29' pd='2*int((nf+1)/2) * (W/nf + 0.29)' ps='2*int((nf+2)/2) * (W/nf + 0.29)'
+ nrd='0.29 / W' nrs='0.29 / W' sa=0 sb=0 sd=0 mult=1 m=1
XM3[13] net1[13] Vout VSS VDD sky130_fd_pr__pfet_01v8_lvt L=1 W=7 nf=1 ad='int((nf+1)/2) * W/nf * 0.29'
+ as='int((nf+2)/2) * W/nf * 0.29' pd='2*int((nf+1)/2) * (W/nf + 0.29)' ps='2*int((nf+2)/2) * (W/nf + 0.29)'
+ nrd='0.29 / W' nrs='0.29 / W' sa=0 sb=0 sd=0 mult=1 m=1
XM3[12] net1[12] Vout VSS VDD sky130_fd_pr__pfet_01v8_lvt L=1 W=7 nf=1 ad='int((nf+1)/2) * W/nf * 0.29'
+ as='int((nf+2)/2) * W/nf * 0.29' pd='2*int((nf+1)/2) * (W/nf + 0.29)' ps='2*int((nf+2)/2) * (W/nf + 0.29)'
+ nrd='0.29 / W' nrs='0.29 / W' sa=0 sb=0 sd=0 mult=1 m=1
XM3[11] net1[11] Vout VSS VDD sky130_fd_pr__pfet_01v8_lvt L=1 W=7 nf=1 ad='int((nf+1)/2) * W/nf * 0.29'
+ as='int((nf+2)/2) * W/nf * 0.29' pd='2*int((nf+1)/2) * (W/nf + 0.29)' ps='2*int((nf+2)/2) * (W/nf + 0.29)'
+ nrd='0.29 / W' nrs='0.29 / W' sa=0 sb=0 sd=0 mult=1 m=1
XM3[10] net1[10] Vout VSS VDD sky130_fd_pr__pfet_01v8_lvt L=1 W=7 nf=1 ad='int((nf+1)/2) * W/nf * 0.29'
+ as='int((nf+2)/2) * W/nf * 0.29' pd='2*int((nf+1)/2) * (W/nf + 0.29)' ps='2*int((nf+2)/2) * (W/nf + 0.29)'
+ nrd='0.29 / W' nrs='0.29 / W' sa=0 sb=0 sd=0 mult=1 m=1
XM3[9] net1[9] Vout VSS VDD sky130_fd_pr__pfet_01v8_lvt L=1 W=7 nf=1 ad='int((nf+1)/2) * W/nf * 0.29'
+ as='int((nf+2)/2) * W/nf * 0.29' pd='2*int((nf+1)/2) * (W/nf + 0.29)' ps='2*int((nf+2)/2) * (W/nf + 0.29)'
+ nrd='0.29 / W' nrs='0.29 / W' sa=0 sb=0 sd=0 mult=1 m=1
XM3[8] net1[8] Vout VSS VDD sky130_fd_pr__pfet_01v8_lvt L=1 W=7 nf=1 ad='int((nf+1)/2) * W/nf * 0.29'
+ as='int((nf+2)/2) * W/nf * 0.29' pd='2*int((nf+1)/2) * (W/nf + 0.29)' ps='2*int((nf+2)/2) * (W/nf + 0.29)'
+ nrd='0.29 / W' nrs='0.29 / W' sa=0 sb=0 sd=0 mult=1 m=1
XM3[7] net1[7] Vout VSS VDD sky130_fd_pr__pfet_01v8_lvt L=1 W=7 nf=1 ad='int((nf+1)/2) * W/nf * 0.29'
+ as='int((nf+2)/2) * W/nf * 0.29' pd='2*int((nf+1)/2) * (W/nf + 0.29)' ps='2*int((nf+2)/2) * (W/nf + 0.29)'
+ nrd='0.29 / W' nrs='0.29 / W' sa=0 sb=0 sd=0 mult=1 m=1
XM3[6] net1[6] Vout VSS VDD sky130_fd_pr__pfet_01v8_lvt L=1 W=7 nf=1 ad='int((nf+1)/2) * W/nf * 0.29'
+ as='int((nf+2)/2) * W/nf * 0.29' pd='2*int((nf+1)/2) * (W/nf + 0.29)' ps='2*int((nf+2)/2) * (W/nf + 0.29)'
+ nrd='0.29 / W' nrs='0.29 / W' sa=0 sb=0 sd=0 mult=1 m=1
XM3[5] net1[5] Vout VSS VDD sky130_fd_pr__pfet_01v8_lvt L=1 W=7 nf=1 ad='int((nf+1)/2) * W/nf * 0.29'
+ as='int((nf+2)/2) * W/nf * 0.29' pd='2*int((nf+1)/2) * (W/nf + 0.29)' ps='2*int((nf+2)/2) * (W/nf + 0.29)'
+ nrd='0.29 / W' nrs='0.29 / W' sa=0 sb=0 sd=0 mult=1 m=1
XM3[4] net1[4] Vout VSS VDD sky130_fd_pr__pfet_01v8_lvt L=1 W=7 nf=1 ad='int((nf+1)/2) * W/nf * 0.29'
+ as='int((nf+2)/2) * W/nf * 0.29' pd='2*int((nf+1)/2) * (W/nf + 0.29)' ps='2*int((nf+2)/2) * (W/nf + 0.29)'
+ nrd='0.29 / W' nrs='0.29 / W' sa=0 sb=0 sd=0 mult=1 m=1
XM3[3] net1[3] Vout VSS VDD sky130_fd_pr__pfet_01v8_lvt L=1 W=7 nf=1 ad='int((nf+1)/2) * W/nf * 0.29'
+ as='int((nf+2)/2) * W/nf * 0.29' pd='2*int((nf+1)/2) * (W/nf + 0.29)' ps='2*int((nf+2)/2) * (W/nf + 0.29)'
+ nrd='0.29 / W' nrs='0.29 / W' sa=0 sb=0 sd=0 mult=1 m=1
XM3[2] net1[2] Vout VSS VDD sky130_fd_pr__pfet_01v8_lvt L=1 W=7 nf=1 ad='int((nf+1)/2) * W/nf * 0.29'
+ as='int((nf+2)/2) * W/nf * 0.29' pd='2*int((nf+1)/2) * (W/nf + 0.29)' ps='2*int((nf+2)/2) * (W/nf + 0.29)'
+ nrd='0.29 / W' nrs='0.29 / W' sa=0 sb=0 sd=0 mult=1 m=1
XM3[1] net1[1] Vout VSS VDD sky130_fd_pr__pfet_01v8_lvt L=1 W=7 nf=1 ad='int((nf+1)/2) * W/nf * 0.29'
+ as='int((nf+2)/2) * W/nf * 0.29' pd='2*int((nf+1)/2) * (W/nf + 0.29)' ps='2*int((nf+2)/2) * (W/nf + 0.29)'
+ nrd='0.29 / W' nrs='0.29 / W' sa=0 sb=0 sd=0 mult=1 m=1
XM3[0] net1[0] Vout VSS VDD sky130_fd_pr__pfet_01v8_lvt L=1 W=7 nf=1 ad='int((nf+1)/2) * W/nf * 0.29'
+ as='int((nf+2)/2) * W/nf * 0.29' pd='2*int((nf+1)/2) * (W/nf + 0.29)' ps='2*int((nf+2)/2) * (W/nf + 0.29)'
+ nrd='0.29 / W' nrs='0.29 / W' sa=0 sb=0 sd=0 mult=1 m=1
XM4[1] Vout Vin net2[1] VSS sky130_fd_pr__nfet_01v8_lvt L=1 W=5 nf=1 ad='int((nf+1)/2) * W/nf * 0.29'
+ as='int((nf+2)/2) * W/nf * 0.29' pd='2*int((nf+1)/2) * (W/nf + 0.29)' ps='2*int((nf+2)/2) * (W/nf + 0.29)'
+ nrd='0.29 / W' nrs='0.29 / W' sa=0 sb=0 sd=0 mult=1 m=1
XM4[0] Vout Vin net2[0] VSS sky130_fd_pr__nfet_01v8_lvt L=1 W=5 nf=1 ad='int((nf+1)/2) * W/nf * 0.29'
+ as='int((nf+2)/2) * W/nf * 0.29' pd='2*int((nf+1)/2) * (W/nf + 0.29)' ps='2*int((nf+2)/2) * (W/nf + 0.29)'
+ nrd='0.29 / W' nrs='0.29 / W' sa=0 sb=0 sd=0 mult=1 m=1
XM5[7] net2[1] Vin VSS VSS sky130_fd_pr__nfet_01v8_lvt L=1 W=5 nf=1 ad='int((nf+1)/2) * W/nf * 0.29'
+ as='int((nf+2)/2) * W/nf * 0.29' pd='2*int((nf+1)/2) * (W/nf + 0.29)' ps='2*int((nf+2)/2) * (W/nf + 0.29)'
+ nrd='0.29 / W' nrs='0.29 / W' sa=0 sb=0 sd=0 mult=1 m=1
XM5[6] net2[0] Vin VSS VSS sky130_fd_pr__nfet_01v8_lvt L=1 W=5 nf=1 ad='int((nf+1)/2) * W/nf * 0.29'
+ as='int((nf+2)/2) * W/nf * 0.29' pd='2*int((nf+1)/2) * (W/nf + 0.29)' ps='2*int((nf+2)/2) * (W/nf + 0.29)'
+ nrd='0.29 / W' nrs='0.29 / W' sa=0 sb=0 sd=0 mult=1 m=1
XM5[5] net2[1] Vin VSS VSS sky130_fd_pr__nfet_01v8_lvt L=1 W=5 nf=1 ad='int((nf+1)/2) * W/nf * 0.29'
+ as='int((nf+2)/2) * W/nf * 0.29' pd='2*int((nf+1)/2) * (W/nf + 0.29)' ps='2*int((nf+2)/2) * (W/nf + 0.29)'
+ nrd='0.29 / W' nrs='0.29 / W' sa=0 sb=0 sd=0 mult=1 m=1
XM5[4] net2[0] Vin VSS VSS sky130_fd_pr__nfet_01v8_lvt L=1 W=5 nf=1 ad='int((nf+1)/2) * W/nf * 0.29'
+ as='int((nf+2)/2) * W/nf * 0.29' pd='2*int((nf+1)/2) * (W/nf + 0.29)' ps='2*int((nf+2)/2) * (W/nf + 0.29)'
+ nrd='0.29 / W' nrs='0.29 / W' sa=0 sb=0 sd=0 mult=1 m=1
XM5[3] net2[1] Vin VSS VSS sky130_fd_pr__nfet_01v8_lvt L=1 W=5 nf=1 ad='int((nf+1)/2) * W/nf * 0.29'
+ as='int((nf+2)/2) * W/nf * 0.29' pd='2*int((nf+1)/2) * (W/nf + 0.29)' ps='2*int((nf+2)/2) * (W/nf + 0.29)'
+ nrd='0.29 / W' nrs='0.29 / W' sa=0 sb=0 sd=0 mult=1 m=1
XM5[2] net2[0] Vin VSS VSS sky130_fd_pr__nfet_01v8_lvt L=1 W=5 nf=1 ad='int((nf+1)/2) * W/nf * 0.29'
+ as='int((nf+2)/2) * W/nf * 0.29' pd='2*int((nf+1)/2) * (W/nf + 0.29)' ps='2*int((nf+2)/2) * (W/nf + 0.29)'
+ nrd='0.29 / W' nrs='0.29 / W' sa=0 sb=0 sd=0 mult=1 m=1
XM5[1] net2[1] Vin VSS VSS sky130_fd_pr__nfet_01v8_lvt L=1 W=5 nf=1 ad='int((nf+1)/2) * W/nf * 0.29'
+ as='int((nf+2)/2) * W/nf * 0.29' pd='2*int((nf+1)/2) * (W/nf + 0.29)' ps='2*int((nf+2)/2) * (W/nf + 0.29)'
+ nrd='0.29 / W' nrs='0.29 / W' sa=0 sb=0 sd=0 mult=1 m=1
XM5[0] net2[0] Vin VSS VSS sky130_fd_pr__nfet_01v8_lvt L=1 W=5 nf=1 ad='int((nf+1)/2) * W/nf * 0.29'
+ as='int((nf+2)/2) * W/nf * 0.29' pd='2*int((nf+1)/2) * (W/nf + 0.29)' ps='2*int((nf+2)/2) * (W/nf + 0.29)'
+ nrd='0.29 / W' nrs='0.29 / W' sa=0 sb=0 sd=0 mult=1 m=1
XM6[3] VDD Vout net2[1] VSS sky130_fd_pr__nfet_01v8_lvt L=1 W=5 nf=1 ad='int((nf+1)/2) * W/nf * 0.29'
+ as='int((nf+2)/2) * W/nf * 0.29' pd='2*int((nf+1)/2) * (W/nf + 0.29)' ps='2*int((nf+2)/2) * (W/nf + 0.29)'
+ nrd='0.29 / W' nrs='0.29 / W' sa=0 sb=0 sd=0 mult=1 m=1
XM6[2] VDD Vout net2[0] VSS sky130_fd_pr__nfet_01v8_lvt L=1 W=5 nf=1 ad='int((nf+1)/2) * W/nf * 0.29'
+ as='int((nf+2)/2) * W/nf * 0.29' pd='2*int((nf+1)/2) * (W/nf + 0.29)' ps='2*int((nf+2)/2) * (W/nf + 0.29)'
+ nrd='0.29 / W' nrs='0.29 / W' sa=0 sb=0 sd=0 mult=1 m=1
XM6[1] VDD Vout net2[1] VSS sky130_fd_pr__nfet_01v8_lvt L=1 W=5 nf=1 ad='int((nf+1)/2) * W/nf * 0.29'
+ as='int((nf+2)/2) * W/nf * 0.29' pd='2*int((nf+1)/2) * (W/nf + 0.29)' ps='2*int((nf+2)/2) * (W/nf + 0.29)'
+ nrd='0.29 / W' nrs='0.29 / W' sa=0 sb=0 sd=0 mult=1 m=1
XM6[0] VDD Vout net2[0] VSS sky130_fd_pr__nfet_01v8_lvt L=1 W=5 nf=1 ad='int((nf+1)/2) * W/nf * 0.29'
+ as='int((nf+2)/2) * W/nf * 0.29' pd='2*int((nf+1)/2) * (W/nf + 0.29)' ps='2*int((nf+2)/2) * (W/nf + 0.29)'
+ nrd='0.29 / W' nrs='0.29 / W' sa=0 sb=0 sd=0 mult=1 m=1
.ends

.end
